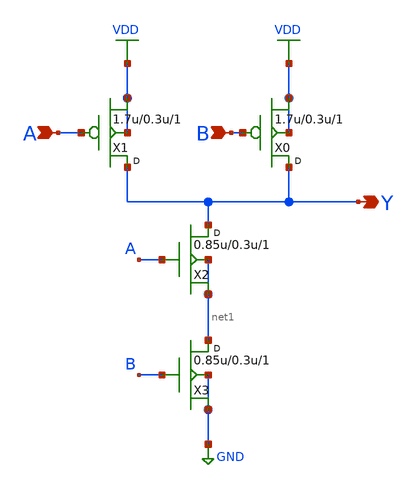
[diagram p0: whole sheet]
** sch_path: xschem/9t_nand2_1.sch
**.subckt 9t_nand2_1 A B Y
*.ipin A
*.ipin B
*.opin Y
X1 Y A VDD VDD pfet_03p3 w=1.7u l=0.3u m=1
X0 Y B VDD VDD pfet_03p3 w=1.7u l=0.3u m=1
X2 Y A net1 net1 nfet_03p3 w=0.85u l=0.3u m=1
X3 net1 B GND GND nfet_03p3 w=0.85u l=0.3u m=1
**.ends
.GLOBAL VDD
.GLOBAL GND
.end
